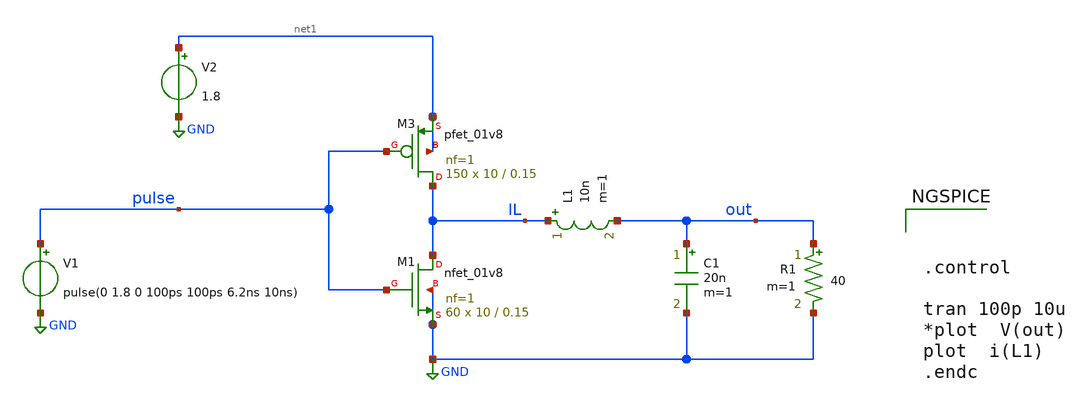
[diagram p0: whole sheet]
** sch_path: xschem/DC_DC_Converter_xschem/OTHERS/DC_DC_Converter_6/TOP_LEVEL/buck_synchronous.sch
**.subckt buck_synchronous
XM3 IL pulse net1 net1 sky130_fd_pr__pfet_01v8 L=0.15 W=10 nf=1 ad='int((nf+1)/2) * W/nf * 0.29' as='int((nf+2)/2) * W/nf * 0.29'
+ pd='2*int((nf+1)/2) * (W/nf + 0.29)' ps='2*int((nf+2)/2) * (W/nf + 0.29)' nrd='0.29 / W' nrs='0.29 / W'
+ sa=0 sb=0 sd=0 mult=150 m=150
XM1 IL pulse GND GND sky130_fd_pr__nfet_01v8 L=0.15 W=10 nf=1 ad='int((nf+1)/2) * W/nf * 0.29' as='int((nf+2)/2) * W/nf * 0.29'
+ pd='2*int((nf+1)/2) * (W/nf + 0.29)' ps='2*int((nf+2)/2) * (W/nf + 0.29)' nrd='0.29 / W' nrs='0.29 / W'
+ sa=0 sb=0 sd=0 mult=60 m=60
V2 net1 GND 1.8
L1 IL out 10n m=1
C1 out GND 20n m=1
R1 out GND 40 m=1
V1 pulse GND pulse(0 1.8 0 100ps 100ps 6.2ns 10ns)
**** begin user architecture code

** opencircuitdesign pdks install
.lib $::SKYWATER_MODELS/sky130.lib.spice tt





.control

tran 100p 10u
*plot  V(out)
plot  i(L1)
.endc


**** end user architecture code
**.ends
.GLOBAL GND
.end
